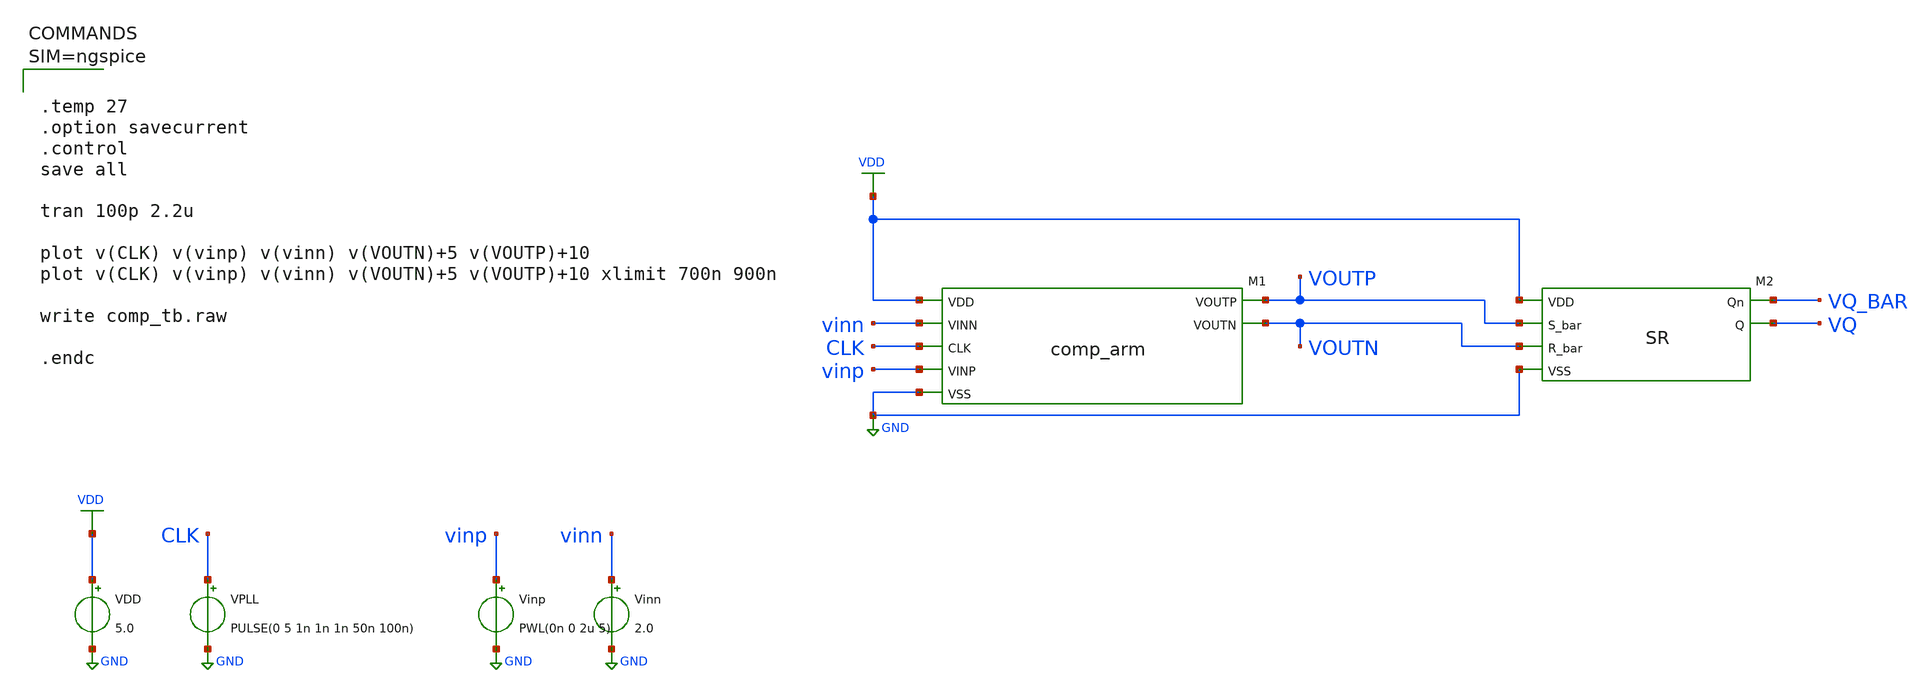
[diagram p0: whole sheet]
** sch_path: xschem/comp_arm_tb.sch
**.subckt comp_arm_tb
VDD VDD GND 5.0
VPLL CLK GND PULSE(0 5 1n 1n 1n 50n 100n)
Vinn vinn GND 2.0
Vinp vinp GND PWL(0n 0 2u 5)
XM2 VDD VQ_BAR VQ VOUTN VOUTP GND SR
XM1 VOUTP VDD vinp vinn CLK GND VOUTN comp_arm
**** begin user architecture code



.temp 27
.option savecurrent
.control
save all

tran 100p 2.2u

plot v(CLK) v(vinp) v(vinn) v(VOUTN)+5 v(VOUTP)+10
plot v(CLK) v(vinp) v(vinn) v(VOUTN)+5 v(VOUTP)+10 xlimit 700n 900n

write comp_tb.raw

.endc




** opencircuitdesign pdks install
.lib $::SKYWATER_MODELS/sky130.lib.spice tt

**** end user architecture code
**.ends

* expanding   symbol:  SR.sym # of pins=6
** sym_path: xschem/SR.sym
** sch_path: xschem/SR.sch
.subckt SR VDD Qn Q R_bar S_bar VSS


*.iopin VDD
*.opin Qn
*.opin Q
*.ipin S_bar
*.ipin R_bar
*.iopin VSS
XM7 Q Qn VDD VDD sky130_fd_pr__pfet_g5v0d10v5 L=0.5 W=6 nf=1 ad='int((1 + 1)/2) * 6 / 1 * 0.29' as='int((1 + 2)/2) * 6 / 1 * 0.29'
+ pd='2*int((1 + 1)/2) * (6 / 1 + 0.29)' ps='2*int((1 + 2)/2) * (6 / 1 + 0.29)' nrd='0.29 / 6 ' nrs='0.29 / 6 '
+ sa=0 sb=0 sd=0 mult=1 m=1
XM8 Q S_bar VDD VDD sky130_fd_pr__pfet_g5v0d10v5 L=0.5 W=6 nf=1 ad='int((1 + 1)/2) * 6 / 1 * 0.29' as='int((1 + 2)/2) * 6 / 1 * 0.29'
+ pd='2*int((1 + 1)/2) * (6 / 1 + 0.29)' ps='2*int((1 + 2)/2) * (6 / 1 + 0.29)' nrd='0.29 / 6 ' nrs='0.29 / 6 '
+ sa=0 sb=0 sd=0 mult=1 m=1
XM15 Q S_bar net1 VSS sky130_fd_pr__nfet_g5v0d10v5 L=0.5 W=3 nf=1 ad='int((1 + 1)/2) * 3 / 1 * 0.29'
+ as='int((1 + 2)/2) * 3 / 1 * 0.29' pd='2*int((1 + 1)/2) * (3 / 1 + 0.29)' ps='2*int((1 + 2)/2) * (3 / 1 + 0.29)'
+ nrd='0.29 / 3 ' nrs='0.29 / 3 ' sa=0 sb=0 sd=0 mult=1 m=1
XM16 net1 Qn VSS VSS sky130_fd_pr__nfet_g5v0d10v5 L=0.5 W=3 nf=1 ad='int((1 + 1)/2) * 3 / 1 * 0.29' as='int((1 + 2)/2) * 3 / 1 * 0.29'
+ pd='2*int((1 + 1)/2) * (3 / 1 + 0.29)' ps='2*int((1 + 2)/2) * (3 / 1 + 0.29)' nrd='0.29 / 3 ' nrs='0.29 / 3 '
+ sa=0 sb=0 sd=0 mult=1 m=1
XM17 Qn R_bar VDD VDD sky130_fd_pr__pfet_g5v0d10v5 L=0.5 W=6 nf=1 ad='int((1 + 1)/2) * 6 / 1 * 0.29'
+ as='int((1 + 2)/2) * 6 / 1 * 0.29' pd='2*int((1 + 1)/2) * (6 / 1 + 0.29)' ps='2*int((1 + 2)/2) * (6 / 1 + 0.29)'
+ nrd='0.29 / 6 ' nrs='0.29 / 6 ' sa=0 sb=0 sd=0 mult=1 m=1
XM18 Qn Q VDD VDD sky130_fd_pr__pfet_g5v0d10v5 L=0.5 W=6 nf=1 ad='int((1 + 1)/2) * 6 / 1 * 0.29' as='int((1 + 2)/2) * 6 / 1 * 0.29'
+ pd='2*int((1 + 1)/2) * (6 / 1 + 0.29)' ps='2*int((1 + 2)/2) * (6 / 1 + 0.29)' nrd='0.29 / 6 ' nrs='0.29 / 6 '
+ sa=0 sb=0 sd=0 mult=1 m=1
XM23 Qn Q net2 VSS sky130_fd_pr__nfet_g5v0d10v5 L=0.5 W=3 nf=1 ad='int((1 + 1)/2) * 3 / 1 * 0.29' as='int((1 + 2)/2) * 3 / 1 * 0.29'
+ pd='2*int((1 + 1)/2) * (3 / 1 + 0.29)' ps='2*int((1 + 2)/2) * (3 / 1 + 0.29)' nrd='0.29 / 3 ' nrs='0.29 / 3 '
+ sa=0 sb=0 sd=0 mult=1 m=1
XM27 net2 R_bar VSS VSS sky130_fd_pr__nfet_g5v0d10v5 L=0.5 W=3 nf=1 ad='int((1 + 1)/2) * 3 / 1 * 0.29'
+ as='int((1 + 2)/2) * 3 / 1 * 0.29' pd='2*int((1 + 1)/2) * (3 / 1 + 0.29)' ps='2*int((1 + 2)/2) * (3 / 1 + 0.29)'
+ nrd='0.29 / 3 ' nrs='0.29 / 3 ' sa=0 sb=0 sd=0 mult=1 m=1
.ends


* expanding   symbol:  comp_arm.sym # of pins=7
** sym_path: xschem/comp_arm.sym
** sch_path: xschem/comp_arm.sch
.subckt comp_arm VOUTP VDD VINP VINN CLK VSS VOUTN

*.iopin VSS
*.iopin VDD
*.ipin CLK
*.ipin VINP
*.ipin VINN
*.opin VOUTN
*.opin VOUTP
XM1 net1 CLK VDD VDD sky130_fd_pr__pfet_g5v0d10v5 L=0.5 W=30 nf=1 ad='int((1 + 1)/2) * 30 / 1 * 0.29'
+ as='int((1 + 2)/2) * 30 / 1 * 0.29' pd='2*int((1 + 1)/2) * (30 / 1 + 0.29)' ps='2*int((1 + 2)/2) * (30 / 1 + 0.29)'
+ nrd='0.29 / 30 ' nrs='0.29 / 30 ' sa=0 sb=0 sd=0 mult=1 m=1
XM2 VOUTN CLK VDD VDD sky130_fd_pr__pfet_g5v0d10v5 L=0.5 W=30 nf=1 ad='int((1 + 1)/2) * 30 / 1 * 0.29'
+ as='int((1 + 2)/2) * 30 / 1 * 0.29' pd='2*int((1 + 1)/2) * (30 / 1 + 0.29)' ps='2*int((1 + 2)/2) * (30 / 1 + 0.29)'
+ nrd='0.29 / 30 ' nrs='0.29 / 30 ' sa=0 sb=0 sd=0 mult=1 m=1
XM3 VOUTN VOUTP VDD VDD sky130_fd_pr__pfet_g5v0d10v5 L=0.5 W=30 nf=1 ad='int((1 + 1)/2) * 30 / 1 * 0.29'
+ as='int((1 + 2)/2) * 30 / 1 * 0.29' pd='2*int((1 + 1)/2) * (30 / 1 + 0.29)' ps='2*int((1 + 2)/2) * (30 / 1 + 0.29)'
+ nrd='0.29 / 30 ' nrs='0.29 / 30 ' sa=0 sb=0 sd=0 mult=1 m=1
XM4 VOUTP VOUTN VDD VDD sky130_fd_pr__pfet_g5v0d10v5 L=0.5 W=30 nf=1 ad='int((1 + 1)/2) * 30 / 1 * 0.29'
+ as='int((1 + 2)/2) * 30 / 1 * 0.29' pd='2*int((1 + 1)/2) * (30 / 1 + 0.29)' ps='2*int((1 + 2)/2) * (30 / 1 + 0.29)'
+ nrd='0.29 / 30 ' nrs='0.29 / 30 ' sa=0 sb=0 sd=0 mult=1 m=1
XM5 VOUTP CLK VDD VDD sky130_fd_pr__pfet_g5v0d10v5 L=0.5 W=30 nf=1 ad='int((1 + 1)/2) * 30 / 1 * 0.29'
+ as='int((1 + 2)/2) * 30 / 1 * 0.29' pd='2*int((1 + 1)/2) * (30 / 1 + 0.29)' ps='2*int((1 + 2)/2) * (30 / 1 + 0.29)'
+ nrd='0.29 / 30 ' nrs='0.29 / 30 ' sa=0 sb=0 sd=0 mult=1 m=1
XM6 net2 CLK VDD VDD sky130_fd_pr__pfet_g5v0d10v5 L=0.5 W=30 nf=1 ad='int((1 + 1)/2) * 30 / 1 * 0.29'
+ as='int((1 + 2)/2) * 30 / 1 * 0.29' pd='2*int((1 + 1)/2) * (30 / 1 + 0.29)' ps='2*int((1 + 2)/2) * (30 / 1 + 0.29)'
+ nrd='0.29 / 30 ' nrs='0.29 / 30 ' sa=0 sb=0 sd=0 mult=1 m=1
XM7 VOUTN VOUTP net1 VSS sky130_fd_pr__nfet_g5v0d10v5 L=0.5 W=10 nf=1 ad='int((1 + 1)/2) * 10 / 1 * 0.29'
+ as='int((1 + 2)/2) * 10 / 1 * 0.29' pd='2*int((1 + 1)/2) * (10 / 1 + 0.29)' ps='2*int((1 + 2)/2) * (10 / 1 + 0.29)'
+ nrd='0.29 / 10 ' nrs='0.29 / 10 ' sa=0 sb=0 sd=0 mult=1 m=1
XM8 VOUTP VOUTN net2 VSS sky130_fd_pr__nfet_g5v0d10v5 L=0.5 W=10 nf=1 ad='int((1 + 1)/2) * 10 / 1 * 0.29'
+ as='int((1 + 2)/2) * 10 / 1 * 0.29' pd='2*int((1 + 1)/2) * (10 / 1 + 0.29)' ps='2*int((1 + 2)/2) * (10 / 1 + 0.29)'
+ nrd='0.29 / 10 ' nrs='0.29 / 10 ' sa=0 sb=0 sd=0 mult=1 m=1
XM9 net1 VINP net3 VSS sky130_fd_pr__nfet_g5v0d10v5 L=0.5 W=10 nf=1 ad='int((1 + 1)/2) * 10 / 1 * 0.29'
+ as='int((1 + 2)/2) * 10 / 1 * 0.29' pd='2*int((1 + 1)/2) * (10 / 1 + 0.29)' ps='2*int((1 + 2)/2) * (10 / 1 + 0.29)'
+ nrd='0.29 / 10 ' nrs='0.29 / 10 ' sa=0 sb=0 sd=0 mult=1 m=1
XM10 net2 VINN net3 VSS sky130_fd_pr__nfet_g5v0d10v5 L=0.5 W=10 nf=1 ad='int((1 + 1)/2) * 10 / 1 * 0.29'
+ as='int((1 + 2)/2) * 10 / 1 * 0.29' pd='2*int((1 + 1)/2) * (10 / 1 + 0.29)' ps='2*int((1 + 2)/2) * (10 / 1 + 0.29)'
+ nrd='0.29 / 10 ' nrs='0.29 / 10 ' sa=0 sb=0 sd=0 mult=1 m=1
XM11 net3 CLK VSS VSS sky130_fd_pr__nfet_g5v0d10v5 L=0.5 W=10 nf=1 ad='int((1 + 1)/2) * 10 / 1 * 0.29'
+ as='int((1 + 2)/2) * 10 / 1 * 0.29' pd='2*int((1 + 1)/2) * (10 / 1 + 0.29)' ps='2*int((1 + 2)/2) * (10 / 1 + 0.29)'
+ nrd='0.29 / 10 ' nrs='0.29 / 10 ' sa=0 sb=0 sd=0 mult=1 m=1
.ends

.GLOBAL GND
.GLOBAL VDD
.end
